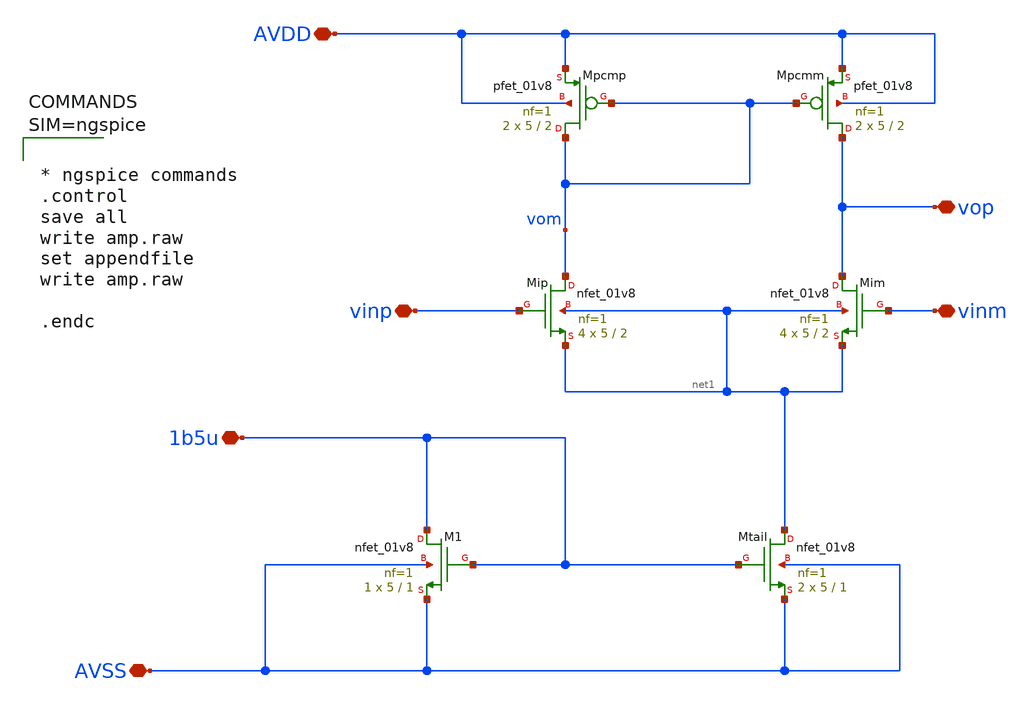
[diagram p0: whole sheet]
** sch_path: work/xschem/amp.sch
**.subckt amp vop vinp vinm 1b5u AVSS AVDD
*.iopin vop
*.iopin vinp
*.iopin vinm
*.iopin 1b5u
*.iopin AVSS
*.iopin AVDD
XMtail net1 1b5u AVSS AVSS sky130_fd_pr__nfet_01v8 L=1 W=5 nf=1 ad='int((1 + 1)/2) * 5 / 1 * 0.29' as='int((1 + 2)/2) * 5 / 1 * 0.29'
+ pd='2*int((1 + 1)/2) * (5 / 1 + 0.29)' ps='2*int((1 + 2)/2) * (5 / 1 + 0.29)' nrd='0.29 / 5 ' nrs='0.29 / 5 '
+ sa=0 sb=0 sd=0 mult=2 m=2
XM1 1b5u 1b5u AVSS AVSS sky130_fd_pr__nfet_01v8 L=1 W=5 nf=1 ad='int((1 + 1)/2) * 5 / 1 * 0.29' as='int((1 + 2)/2) * 5 / 1 * 0.29'
+ pd='2*int((1 + 1)/2) * (5 / 1 + 0.29)' ps='2*int((1 + 2)/2) * (5 / 1 + 0.29)' nrd='0.29 / 5 ' nrs='0.29 / 5 '
+ sa=0 sb=0 sd=0 mult=1 m=1
XMpcmm vop vom AVDD AVDD sky130_fd_pr__pfet_01v8 L=2 W=5 nf=1 ad='int((nf+1)/2) * W/nf * 0.29' as='int((nf+2)/2) * W/nf * 0.29'
+ pd='2*int((nf+1)/2) * (W/nf + 0.29)' ps='2*int((nf+2)/2) * (W/nf + 0.29)' nrd='0.29 / W' nrs='0.29 / W'
+ sa=0 sb=0 sd=0 mult=2 m=2
XMpcmp vom vom AVDD AVDD sky130_fd_pr__pfet_01v8 L=2 W=5 nf=1 ad='int((nf+1)/2) * W/nf * 0.29' as='int((nf+2)/2) * W/nf * 0.29'
+ pd='2*int((nf+1)/2) * (W/nf + 0.29)' ps='2*int((nf+2)/2) * (W/nf + 0.29)' nrd='0.29 / W' nrs='0.29 / W'
+ sa=0 sb=0 sd=0 mult=2 m=2
XMim vop vinm net1 net1 sky130_fd_pr__nfet_01v8 L=2 W=5 nf=1 ad='int((1 + 1)/2) * 5 / 1 * 0.29' as='int((1 + 2)/2) * 5 / 1 * 0.29'
+ pd='2*int((1 + 1)/2) * (5 / 1 + 0.29)' ps='2*int((1 + 2)/2) * (5 / 1 + 0.29)' nrd='0.29 / 5 ' nrs='0.29 / 5 '
+ sa=0 sb=0 sd=0 mult=4 m=4
XMip vom vinp net1 net1 sky130_fd_pr__nfet_01v8 L=2 W=5 nf=1 ad='int((1 + 1)/2) * 5 / 1 * 0.29' as='int((1 + 2)/2) * 5 / 1 * 0.29'
+ pd='2*int((1 + 1)/2) * (5 / 1 + 0.29)' ps='2*int((1 + 2)/2) * (5 / 1 + 0.29)' nrd='0.29 / 5 ' nrs='0.29 / 5 '
+ sa=0 sb=0 sd=0 mult=4 m=4
**** begin user architecture code



* ngspice commands
.control
save all
write amp.raw
set appendfile
write amp.raw

.endc




** opencircuitdesign pdks install
.lib $::SKYWATER_MODELS/sky130.lib.spice tt

**** end user architecture code
**.ends
.end
